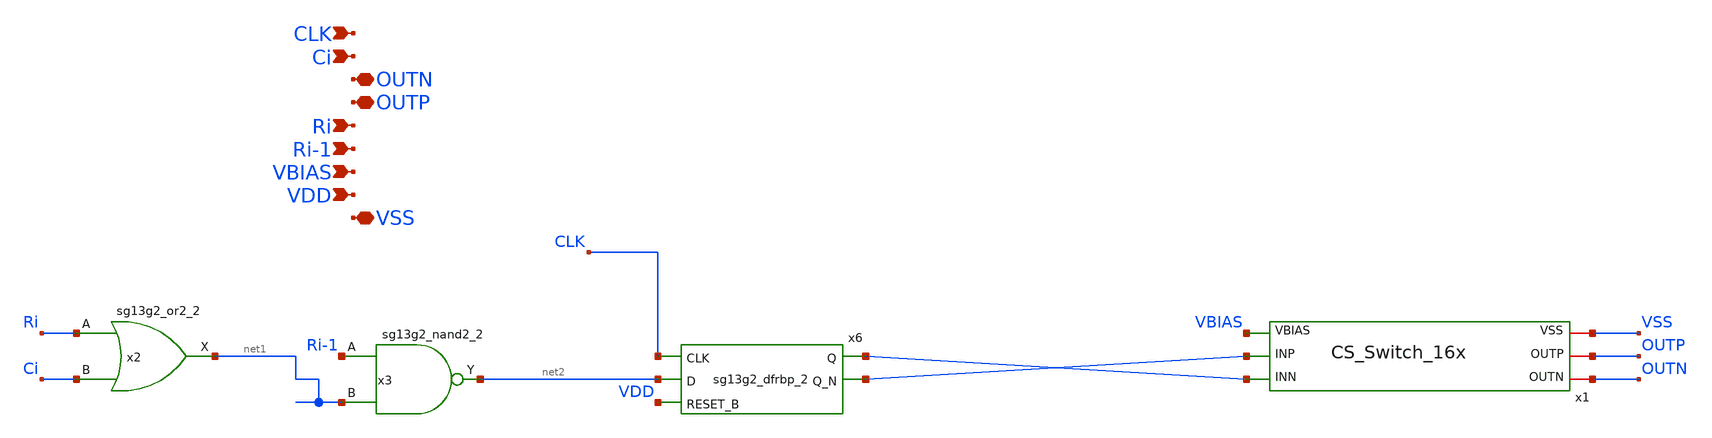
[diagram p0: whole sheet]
** sch_path: dependencies/DAC/DAC-main/schematic/xschem/Unit_cell.sch
**.subckt Unit_cell VSS VDD VBIAS Ri-1 Ri OUTP OUTN Ci CLK
*.iopin VSS
*.ipin VDD
*.ipin VBIAS
*.ipin Ri-1
*.ipin Ri
*.iopin OUTP
*.iopin OUTN
*.ipin Ci
*.ipin CLK
x2 net1 Ri Ci VDD VSS sg13g2_or2_2
x3 net2 Ri-1 net1 VDD VSS sg13g2_nand2_2
x6 net4 net3 CLK net2 VDD VDD VSS sg13g2_dfrbp_2
x1 net4 net3 OUTN OUTP VBIAS VSS CS_Switch_16x
**.ends
.end
